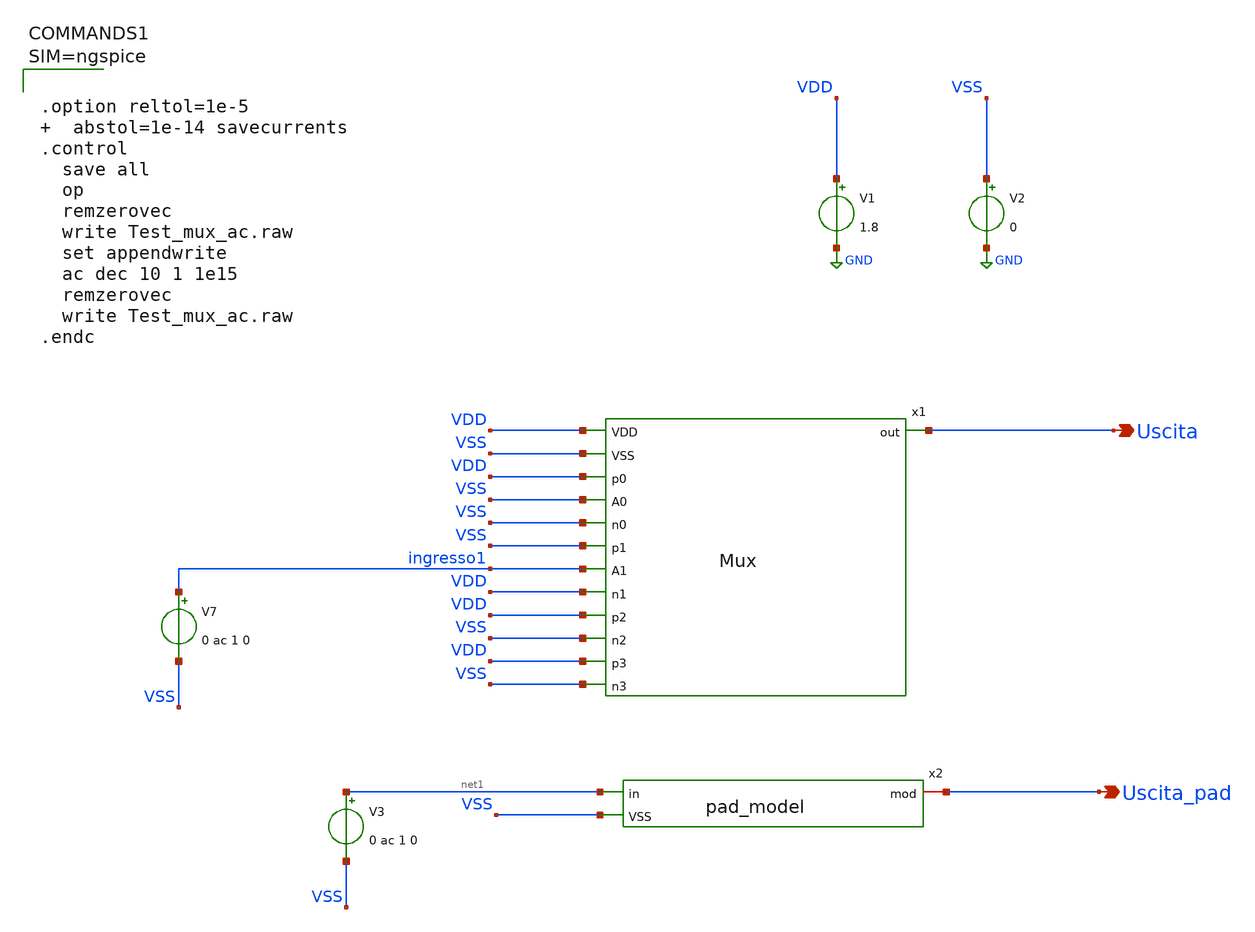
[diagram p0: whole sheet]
** sch_path: xschem/Test_mux_ac.sch
**.subckt Test_mux_ac Uscita Uscita_pad
*.opin Uscita
*.opin Uscita_pad
V1 VDD GND 1.8
V2 VSS GND 0
x1 VDD VSS VDD VSS Uscita VSS VSS ingresso1 VDD VDD VSS VDD VSS Mux
V7 ingresso1 VSS 0 ac 1 0
V3 net1 VSS 0 ac 1 0
x2 Uscita_pad net1 VSS pad_model
**** begin user architecture code

** opencircuitdesign pdks install
.lib $::SKYWATER_MODELS/sky130.lib.spice tt





.option reltol=1e-5   abstol=1e-14 savecurrents
.control
  save all
  op
  remzerovec
  write Test_mux_ac.raw
  set appendwrite
  ac dec 10 1 1e15
  remzerovec
  write Test_mux_ac.raw
.endc



**** end user architecture code
**.ends
.GLOBAL GND
.end
